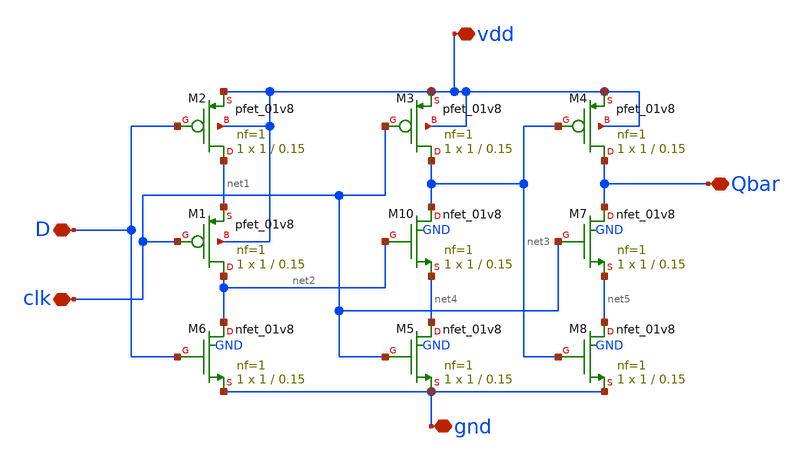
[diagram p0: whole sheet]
** sch_path: tspc.sch
**.subckt tspc vdd gnd D Qbar clk
*.iopin vdd
*.iopin gnd
*.iopin D
*.iopin Qbar
*.iopin clk
XM2 net1 D vdd vdd sky130_fd_pr__pfet_01v8 L=0.15 W=1 nf=1 ad='int((1 + 1)/2) * 1 / 1 * 0.29' as='int((1 + 2)/2) * 1 / 1 * 0.29'
+ pd='2*int((1 + 1)/2) * (1 / 1 + 0.29)' ps='2*int((1 + 2)/2) * (1 / 1 + 0.29)' nrd='0.29 / 1 ' nrs='0.29 / 1 '
+ sa=0 sb=0 sd=0 mult=1 m=1
XM10 net3 net2 net4 GND sky130_fd_pr__nfet_01v8 L=0.15 W=1 nf=1 ad='int((1 + 1)/2) * 1 / 1 * 0.29' as='int((1 + 2)/2) * 1 / 1 * 0.29'
+ pd='2*int((1 + 1)/2) * (1 / 1 + 0.29)' ps='2*int((1 + 2)/2) * (1 / 1 + 0.29)' nrd='0.29 / 1 ' nrs='0.29 / 1 '
+ sa=0 sb=0 sd=0 mult=1 m=1
XM1 net2 clk net1 vdd sky130_fd_pr__pfet_01v8 L=0.15 W=1 nf=1 ad='int((1 + 1)/2) * 1 / 1 * 0.29' as='int((1 + 2)/2) * 1 / 1 * 0.29'
+ pd='2*int((1 + 1)/2) * (1 / 1 + 0.29)' ps='2*int((1 + 2)/2) * (1 / 1 + 0.29)' nrd='0.29 / 1 ' nrs='0.29 / 1 '
+ sa=0 sb=0 sd=0 mult=1 m=1
XM3 net3 clk vdd vdd sky130_fd_pr__pfet_01v8 L=0.15 W=1 nf=1 ad='int((1 + 1)/2) * 1 / 1 * 0.29' as='int((1 + 2)/2) * 1 / 1 * 0.29'
+ pd='2*int((1 + 1)/2) * (1 / 1 + 0.29)' ps='2*int((1 + 2)/2) * (1 / 1 + 0.29)' nrd='0.29 / 1 ' nrs='0.29 / 1 '
+ sa=0 sb=0 sd=0 mult=1 m=1
XM4 Qbar net3 vdd vdd sky130_fd_pr__pfet_01v8 L=0.15 W=1 nf=1 ad='int((1 + 1)/2) * 1 / 1 * 0.29' as='int((1 + 2)/2) * 1 / 1 * 0.29'
+ pd='2*int((1 + 1)/2) * (1 / 1 + 0.29)' ps='2*int((1 + 2)/2) * (1 / 1 + 0.29)' nrd='0.29 / 1 ' nrs='0.29 / 1 '
+ sa=0 sb=0 sd=0 mult=1 m=1
XM5 net4 clk gnd GND sky130_fd_pr__nfet_01v8 L=0.15 W=1 nf=1 ad='int((1 + 1)/2) * 1 / 1 * 0.29' as='int((1 + 2)/2) * 1 / 1 * 0.29'
+ pd='2*int((1 + 1)/2) * (1 / 1 + 0.29)' ps='2*int((1 + 2)/2) * (1 / 1 + 0.29)' nrd='0.29 / 1 ' nrs='0.29 / 1 '
+ sa=0 sb=0 sd=0 mult=1 m=1
XM6 net2 D gnd GND sky130_fd_pr__nfet_01v8 L=0.15 W=1 nf=1 ad='int((1 + 1)/2) * 1 / 1 * 0.29' as='int((1 + 2)/2) * 1 / 1 * 0.29'
+ pd='2*int((1 + 1)/2) * (1 / 1 + 0.29)' ps='2*int((1 + 2)/2) * (1 / 1 + 0.29)' nrd='0.29 / 1 ' nrs='0.29 / 1 '
+ sa=0 sb=0 sd=0 mult=1 m=1
XM7 Qbar clk net5 GND sky130_fd_pr__nfet_01v8 L=0.15 W=1 nf=1 ad='int((1 + 1)/2) * 1 / 1 * 0.29' as='int((1 + 2)/2) * 1 / 1 * 0.29'
+ pd='2*int((1 + 1)/2) * (1 / 1 + 0.29)' ps='2*int((1 + 2)/2) * (1 / 1 + 0.29)' nrd='0.29 / 1 ' nrs='0.29 / 1 '
+ sa=0 sb=0 sd=0 mult=1 m=1
XM8 net5 net3 gnd GND sky130_fd_pr__nfet_01v8 L=0.15 W=1 nf=1 ad='int((1 + 1)/2) * 1 / 1 * 0.29' as='int((1 + 2)/2) * 1 / 1 * 0.29'
+ pd='2*int((1 + 1)/2) * (1 / 1 + 0.29)' ps='2*int((1 + 2)/2) * (1 / 1 + 0.29)' nrd='0.29 / 1 ' nrs='0.29 / 1 '
+ sa=0 sb=0 sd=0 mult=1 m=1
**.ends
.end
